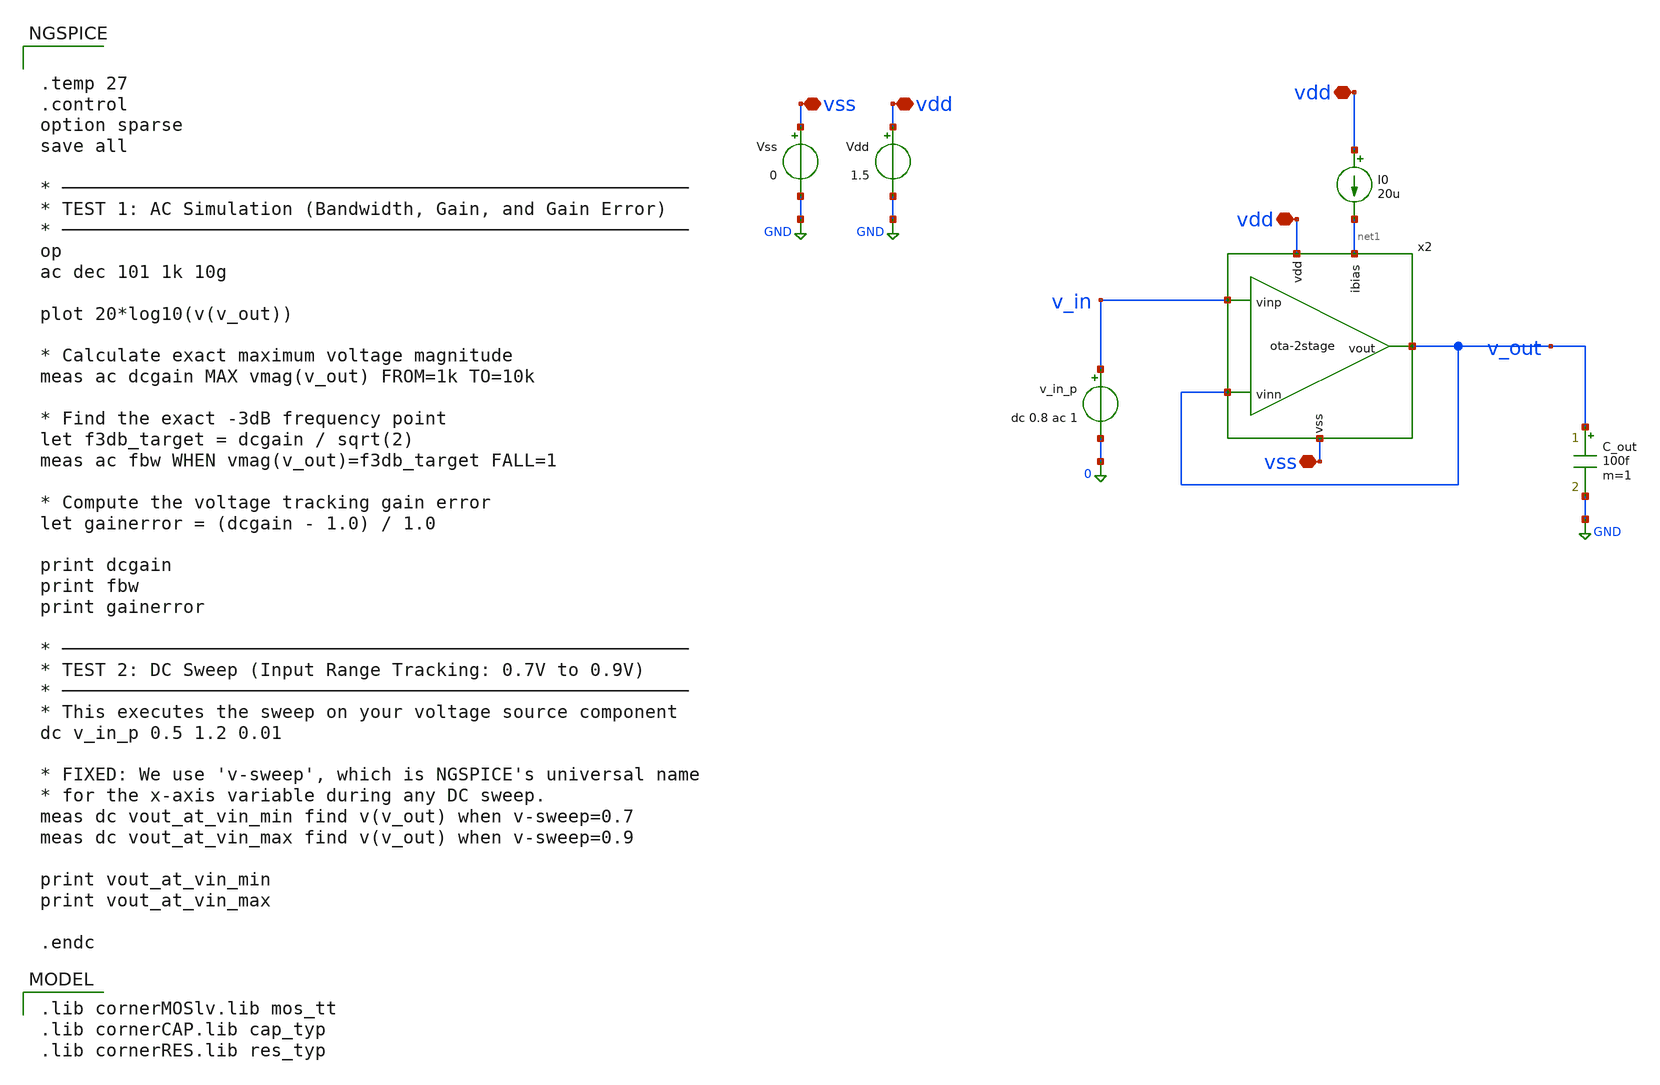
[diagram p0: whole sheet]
** sch_path: Testbench/ota-2stage_tb-vb.sch
**.subckt ota-2stage_tb-vb vss vdd vss vdd vdd
*.iopin vss
*.iopin vdd
*.iopin vss
*.iopin vdd
*.iopin vdd
I0 vdd net1 20u
Vdd vdd GND 1.5
Vss vss GND 0
v_in_p v_in 0 dc 0.8 ac 1
C_out v_out GND 100f m=1
x2 vdd net1 v_out v_out v_in vss ota-2stage
**** begin user architecture code


.temp 27
.control
option sparse
save all

* ─────────────────────────────────────────────────────────
* TEST 1: AC Simulation (Bandwidth, Gain, and Gain Error)
* ─────────────────────────────────────────────────────────
op
ac dec 101 1k 10g

plot 20*log10(v(v_out))

* Calculate exact maximum voltage magnitude
meas ac dcgain MAX vmag(v_out) FROM=1k TO=10k

* Find the exact -3dB frequency point
let f3db_target = dcgain / sqrt(2)
meas ac fbw WHEN vmag(v_out)=f3db_target FALL=1

* Compute the voltage tracking gain error
let gainerror = (dcgain - 1.0) / 1.0

print dcgain
print fbw
print gainerror

* ─────────────────────────────────────────────────────────
* TEST 2: DC Sweep (Input Range Tracking: 0.7V to 0.9V)
* ─────────────────────────────────────────────────────────
* This executes the sweep on your voltage source component
dc v_in_p 0.5 1.2 0.01

* FIXED: We use 'v-sweep', which is NGSPICE's universal name
* for the x-axis variable during any DC sweep.
meas dc vout_at_vin_min find v(v_out) when v-sweep=0.7
meas dc vout_at_vin_max find v(v_out) when v-sweep=0.9

print vout_at_vin_min
print vout_at_vin_max

.endc


 .lib cornerMOSlv.lib mos_tt
.lib cornerCAP.lib cap_typ
.lib cornerRES.lib res_typ

**** end user architecture code
**.ends

* expanding   symbol:  ota-2stage.sym # of pins=6
** sym_path: Testbench/ota-2stage.sym
** sch_path: Testbench/ota-2stage.sch
.subckt ota-2stage vdd ibias vinn vout vinp vss
*.iopin vdd
*.iopin vss
*.ipin ibias
*.iopin vout
*.ipin vinn
*.ipin vinp
XM1 net1 vinn net3 net3 sg13_lv_nmos w=0.5u l=2u ng=1 m=1 mm_ok=1
XM2 net2 vinp net3 net3 sg13_lv_nmos w=0.5u l=2u ng=1 m=1 mm_ok=1
XM4 net2 net1 vdd vdd sg13_lv_pmos w=1u l=2u ng=1 m=1 mm_ok=1
XM3 net1 net1 vdd vdd sg13_lv_pmos w=1u l=2u ng=1 m=1 mm_ok=1
XM5 vout net2 vdd vdd sg13_lv_pmos w=4.5u l=2u ng=1 m=1 mm_ok=1
XM6 ibias ibias vss vss sg13_lv_nmos w=2u l=2u ng=1 m=1 mm_ok=1
XM7 net3 ibias vss vss sg13_lv_nmos w=0.5u l=2u ng=1 m=1 mm_ok=1
XM8 vout ibias vss vss sg13_lv_nmos w=0.5u l=2u ng=1 m=1 mm_ok=1
XCM vout net4 cap_cmim w=11.8e-6 l=11.8e-6 m=1 mm_ok=1
R1 net2 net4 24k m=1
.ends

.GLOBAL GND
.end
